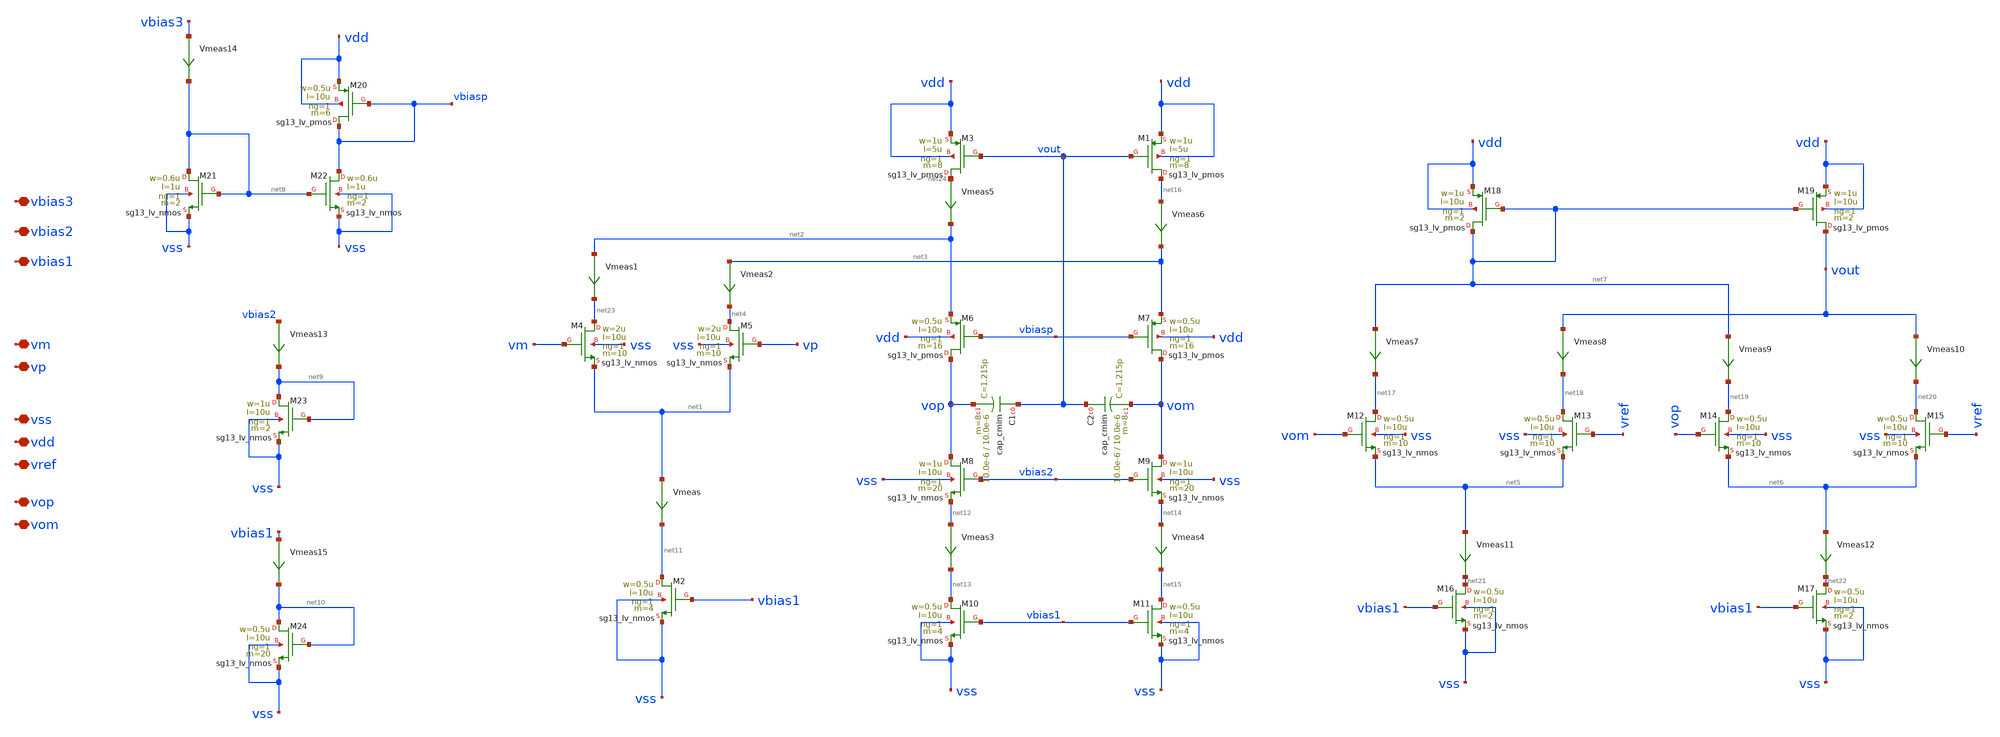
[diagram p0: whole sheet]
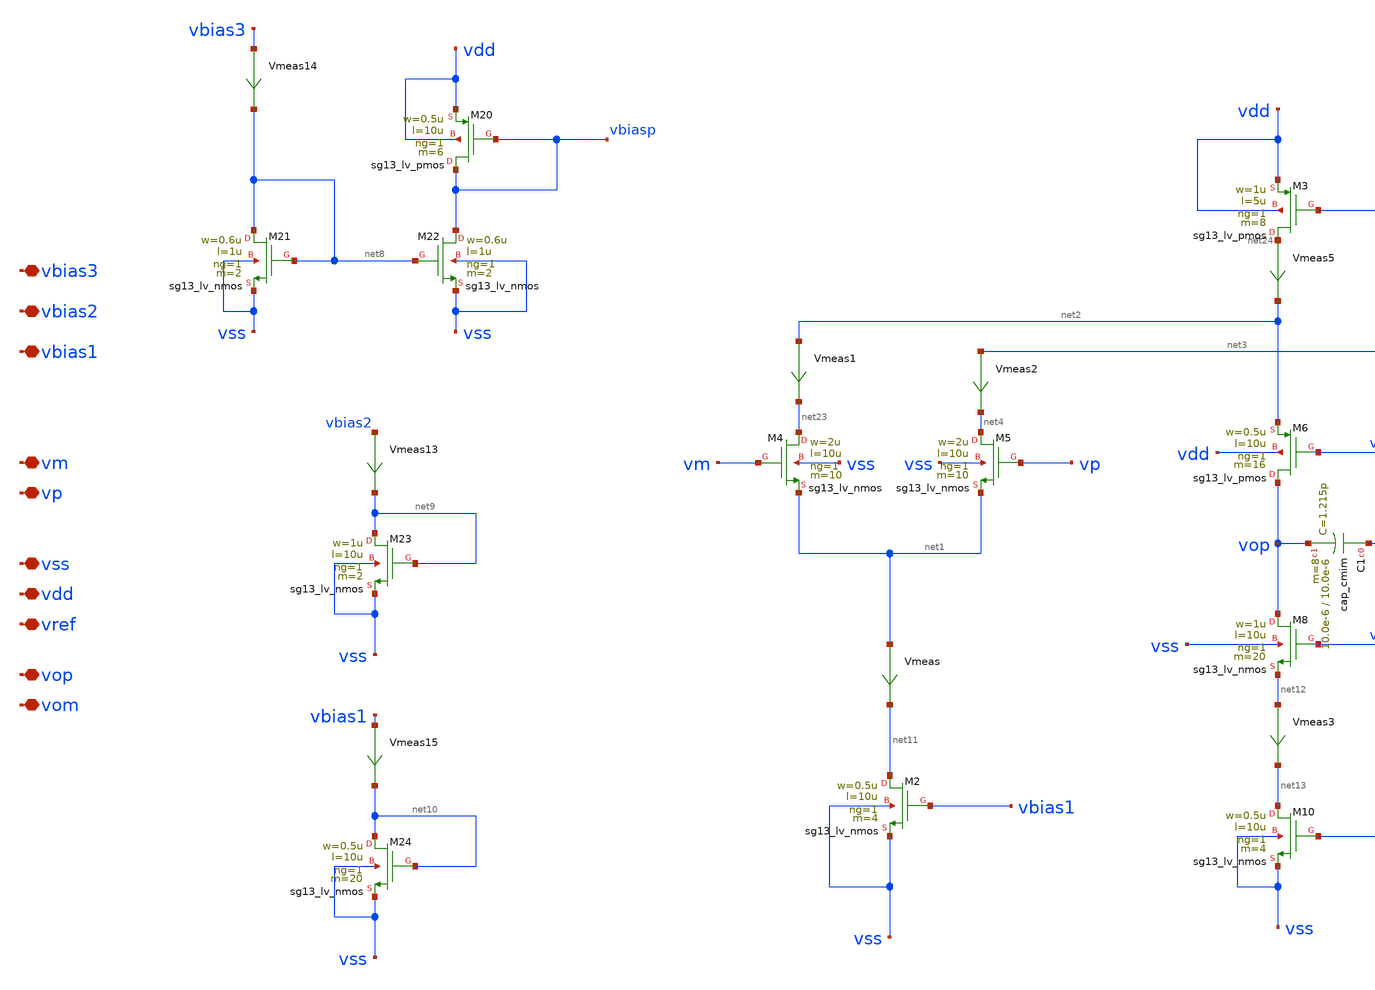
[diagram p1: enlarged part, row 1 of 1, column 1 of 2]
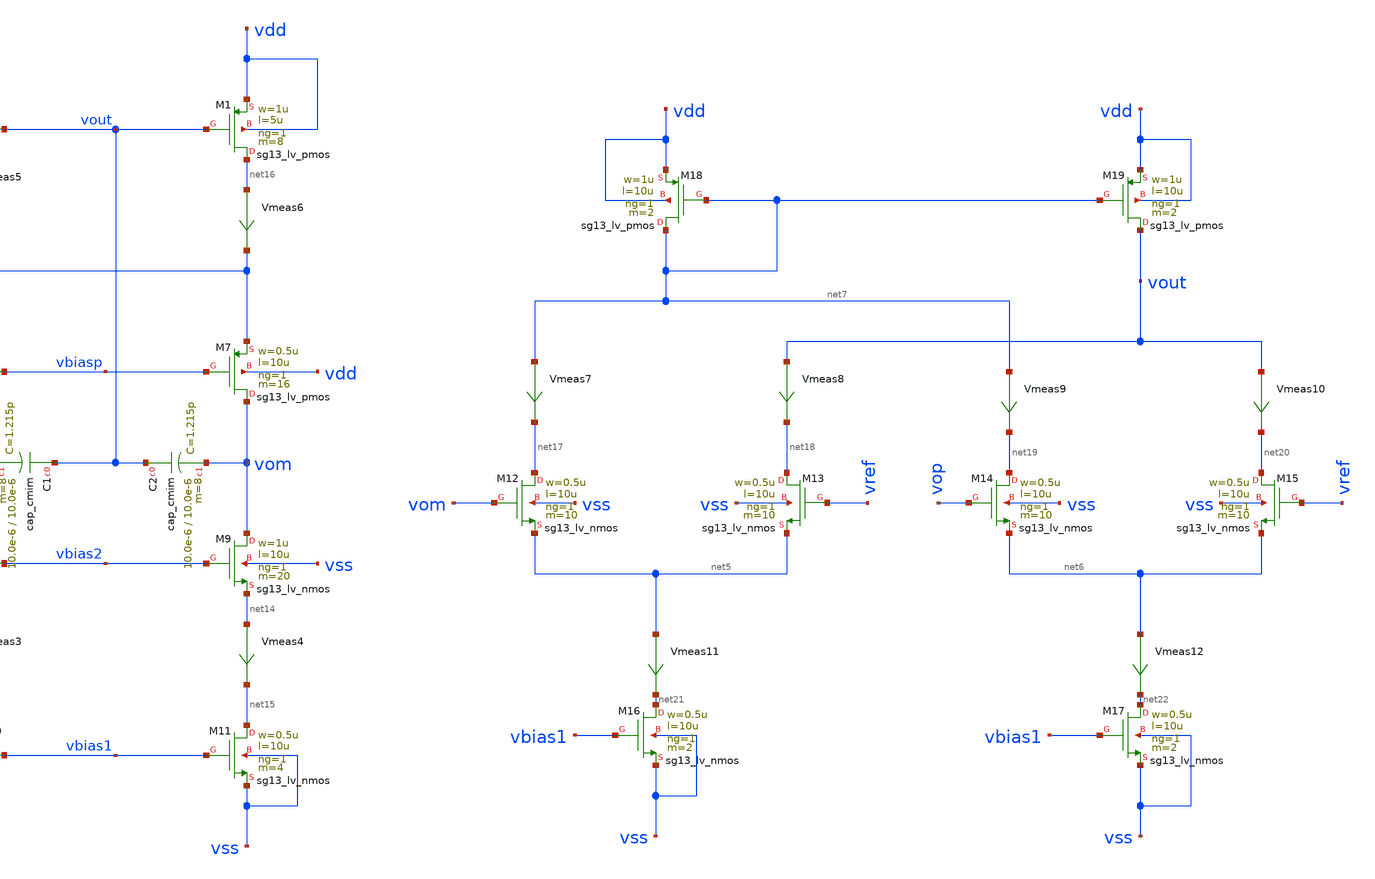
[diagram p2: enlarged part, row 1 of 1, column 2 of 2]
** sch_path: src/Opamp_design/Src/Folded_cascode.sch
**.subckt Folded_cascode vbias3 vbias2 vbias1 vm vp vss vdd vref vop vom
*.iopin vbias3
*.iopin vbias2
*.iopin vbias1
*.iopin vm
*.iopin vp
*.iopin vss
*.iopin vdd
*.iopin vref
*.iopin vop
*.iopin vom
XM1 net16 vout vdd vdd sg13_lv_pmos w=1u l=5u ng=1 m=8 mm_ok=1
XM2 net11 vbias1 vss vss sg13_lv_nmos w=0.5u l=10u ng=1 m=4 mm_ok=1
XM4 net23 vm net1 vss sg13_lv_nmos w=2u l=10u ng=1 m=10 mm_ok=1
XM5 net4 vp net1 vss sg13_lv_nmos w=2u l=10u ng=1 m=10 mm_ok=1
XM3 net24 vout vdd vdd sg13_lv_pmos w=1u l=5u ng=1 m=8 mm_ok=1
XM6 vop vbiasp net2 vdd sg13_lv_pmos w=0.5u l=10u ng=1 m=16 mm_ok=1
XM7 vom vbiasp net3 vdd sg13_lv_pmos w=0.5u l=10u ng=1 m=16 mm_ok=1
XM8 vop vbias2 net12 vss sg13_lv_nmos w=1u l=10u ng=1 m=20 mm_ok=1
XM9 vom vbias2 net14 vss sg13_lv_nmos w=1u l=10u ng=1 m=20 mm_ok=1
XM10 net13 vbias1 vss vss sg13_lv_nmos w=0.5u l=10u ng=1 m=4 mm_ok=1
XM11 net15 vbias1 vss vss sg13_lv_nmos w=0.5u l=10u ng=1 m=4 mm_ok=1
XM12 net17 vom net5 vss sg13_lv_nmos w=0.5u l=10u ng=1 m=10 mm_ok=1
XM13 net18 vref net5 vss sg13_lv_nmos w=0.5u l=10u ng=1 m=10 mm_ok=1
XM14 net19 vop net6 vss sg13_lv_nmos w=0.5u l=10u ng=1 m=10 mm_ok=1
XM15 net20 vref net6 vss sg13_lv_nmos w=0.5u l=10u ng=1 m=10 mm_ok=1
XM16 net21 vbias1 vss vss sg13_lv_nmos w=0.5u l=10u ng=1 m=2 mm_ok=1
XM17 net22 vbias1 vss vss sg13_lv_nmos w=0.5u l=10u ng=1 m=2 mm_ok=1
XM18 net7 net7 vdd vdd sg13_lv_pmos w=1u l=10u ng=1 m=2 mm_ok=1
XM19 vout net7 vdd vdd sg13_lv_pmos w=1u l=10u ng=1 m=2 mm_ok=1
XM20 vbiasp vbiasp vdd vdd sg13_lv_pmos w=0.5u l=10u ng=1 m=6 mm_ok=1
XM21 net8 net8 vss vss sg13_lv_nmos w=0.6u l=1u ng=1 m=2 mm_ok=1
XM22 vbiasp net8 vss vss sg13_lv_nmos w=0.6u l=1u ng=1 m=2 mm_ok=1
XM23 net9 net9 vss vss sg13_lv_nmos w=1u l=10u ng=1 m=2 mm_ok=1
XM24 net10 net10 vss vss sg13_lv_nmos w=0.5u l=10u ng=1 m=20 mm_ok=1
XC1 vout vop cap_cmim w=10.0e-6 l=10.0e-6 m=8 mm_ok=1
XC2 vout vom cap_cmim w=10.0e-6 l=10.0e-6 m=8 mm_ok=1
Vmeas net1 net11 0
.save i(vmeas)
Vmeas3 net12 net13 0
.save i(vmeas3)
Vmeas4 net14 net15 0
.save i(vmeas4)
Vmeas7 net7 net17 0
.save i(vmeas7)
Vmeas8 vout net18 0
.save i(vmeas8)
Vmeas9 net7 net19 0
.save i(vmeas9)
Vmeas10 vout net20 0
.save i(vmeas10)
Vmeas11 net5 net21 0
.save i(vmeas11)
Vmeas12 net6 net22 0
.save i(vmeas12)
Vmeas13 vbias2 net9 0
.save i(vmeas13)
Vmeas14 vbias3 net8 0
.save i(vmeas14)
Vmeas15 vbias1 net10 0
.save i(vmeas15)
Vmeas1 net2 net23 0
.save i(vmeas1)
Vmeas2 net3 net4 0
.save i(vmeas2)
Vmeas5 net24 net2 0
.save i(vmeas5)
Vmeas6 net16 net3 0
.save i(vmeas6)
**.ends
.end
